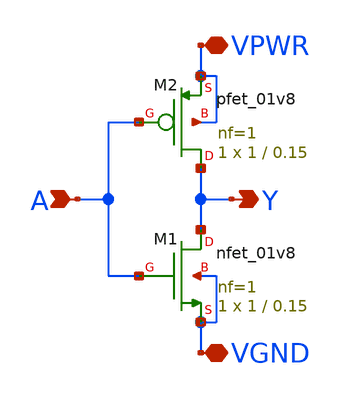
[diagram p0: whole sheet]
** sch_path: xschem/sky130_ef_ip__template.sch
**.subckt sky130_ef_ip__template VPWR VGND A Y
*.iopin VPWR
*.iopin VGND
*.ipin A
*.opin Y
XM1 Y A VGND VGND sky130_fd_pr__nfet_01v8 L=0.15 W=1 nf=1 ad='int((nf+1)/2) * W/nf * 0.29' as='int((nf+2)/2) * W/nf * 0.29'
+ pd='2*int((nf+1)/2) * (W/nf + 0.29)' ps='2*int((nf+2)/2) * (W/nf + 0.29)' nrd='0.29 / W' nrs='0.29 / W'
+ sa=0 sb=0 sd=0 mult=1 m=1
XM2 Y A VPWR VPWR sky130_fd_pr__pfet_01v8 L=0.15 W=1 nf=1 ad='int((nf+1)/2) * W/nf * 0.29' as='int((nf+2)/2) * W/nf * 0.29'
+ pd='2*int((nf+1)/2) * (W/nf + 0.29)' ps='2*int((nf+2)/2) * (W/nf + 0.29)' nrd='0.29 / W' nrs='0.29 / W'
+ sa=0 sb=0 sd=0 mult=1 m=1
**.ends
.end
